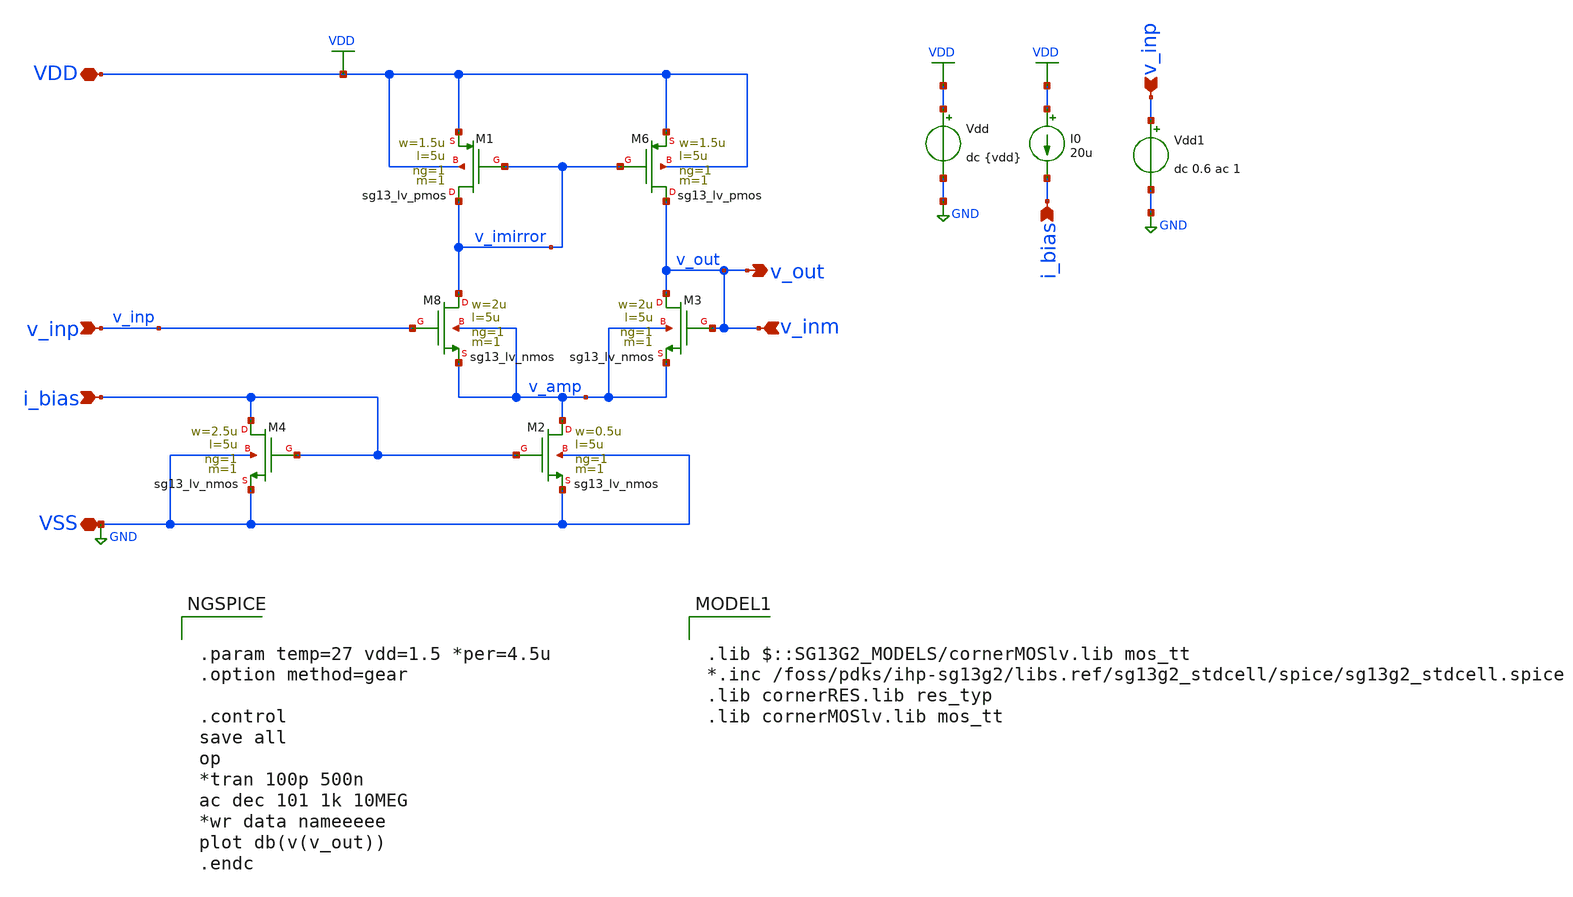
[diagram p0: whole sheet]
** sch_path: 3_Real_Cir/10_Real_Cir/test_Real_Cir/AAAself_build_opamp.sch
**.subckt AAAself_build_opamp v_inp v_inm VDD VSS i_bias i_bias v_inp v_out
*.ipin v_inp
*.ipin v_inm
*.iopin VDD
*.iopin VSS
*.ipin i_bias
*.ipin i_bias
*.ipin v_inp
*.opin v_out
Vdd VDD GND dc {vdd}
XM8 v_imirror v_inp v_amp v_amp sg13_lv_nmos w=2u l=5u ng=1 m=1 mm_ok=1
XM3 v_inm v_inm v_amp v_amp sg13_lv_nmos w=2u l=5u ng=1 m=1 mm_ok=1
XM2 v_amp i_bias VSS VSS sg13_lv_nmos w=0.5u l=5u ng=1 m=1 mm_ok=1
XM4 i_bias i_bias VSS VSS sg13_lv_nmos w=2.5u l=5u ng=1 m=1 mm_ok=1
XM6 v_inm v_imirror VDD VDD sg13_lv_pmos w=1.5u l=5u ng=1 m=1 mm_ok=1
XM1 v_imirror v_imirror VDD VDD sg13_lv_pmos w=1.5u l=5u ng=1 m=1 mm_ok=1
I0 VDD i_bias 20u
Vdd1 v_inp GND dc 0.6 ac 1
**** begin user architecture code

.lib $::SG13G2_MODELS/cornerMOSlv.lib mos_tt
*.inc /foss/pdks/ihp-sg13g2/libs.ref/sg13g2_stdcell/spice/sg13g2_stdcell.spice
.lib cornerRES.lib res_typ
.lib cornerMOSlv.lib mos_tt



.param temp=27 vdd=1.5 *per=4.5u
.option method=gear

.control
save all
op
*tran 100p 500n
ac dec 101 1k 10MEG
*wr data nameeeee
plot db(v(v_out))
.endc


**** end user architecture code
**.ends
.GLOBAL GND
.GLOBAL VDD
.end
